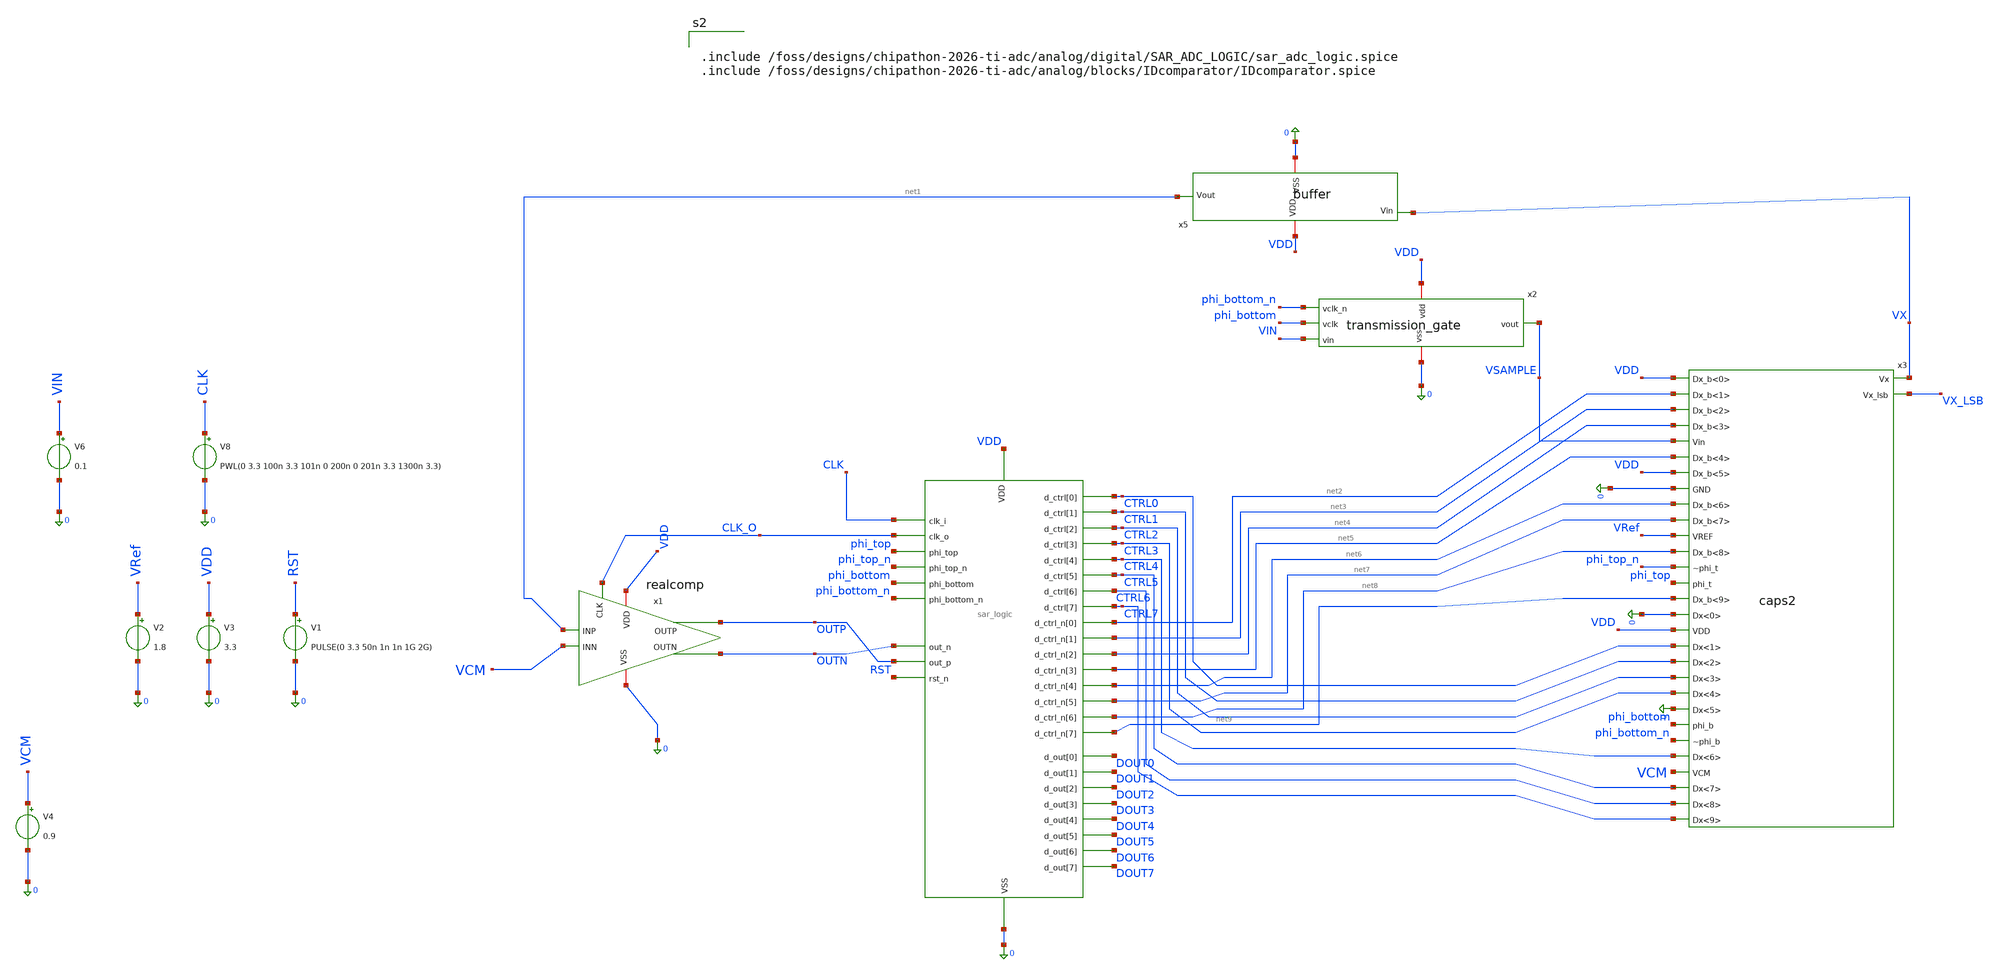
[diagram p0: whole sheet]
** sch_path: analog/top/toptest.sch
**.subckt toptest
V8 CLK 0 PWL(0 3.3 100n 3.3 101n 0 200n 0 201n 3.3 1300n 3.3)
V3 VDD 0 3.3
V1 RST 0 PULSE(0 3.3 50n 1n 1n 1G 2G)
V6 VIN 0 0.1
V2 VRef 0 1.8
V4 VCM 0 0.9
x2 VDD VSAMPLE phi_bottom_n phi_bottom VIN 0 transmission_gate
x3 VDD net2 net3 net4 VSAMPLE net5 VDD 0 net6 net7 VRef net8 phi_top_n phi_top net9 0 VDD CTRL0 VX
+ CTRL1 CTRL2 VX_LSB CTRL3 0 phi_bottom phi_bottom_n CTRL4 VCM CTRL5 CTRL6 CTRL7 caps2
X4 VDD 0 CLK CLK_O CTRL0 CTRL1 CTRL2 CTRL3 CTRL4 CTRL5 CTRL6 CTRL7 net2 net3 net4 net5 net6 net7
+ net8 net9 DOUT0 DOUT1 DOUT2 DOUT3 DOUT4 DOUT5 DOUT6 DOUT7 OUTN OUTP phi_bottom phi_bottom_n phi_top
+ phi_top_n RST sar_adc_logic
x5 VDD VX net1 0 buffer
x1 OUTN OUTP CLK_O 0 VDD net1 VCM realcomp
**** begin user architecture code


.include /foss/designs/chipathon-2026-ti-adc/analog/digital/SAR_ADC_LOGIC/sar_adc_logic.spice
.include /foss/designs/chipathon-2026-ti-adc/analog/blocks/IDcomparator/IDcomparator.spice



.include $::180MCU_MODELS/design.ngspice
.include $PDK_ROOT/gf180mcuD/libs.ref/gf180mcu_fd_sc_mcu7t5v0/spice/gf180mcu_fd_sc_mcu7t5v0.spice
.lib $::180MCU_MODELS/sm141064.ngspice typical
.lib $::180MCU_MODELS/smbb000149.ngspice typical
.lib /foss/pdks/gf180mcuD/libs.tech/ngspice/sm141064.ngspice cap_mim
.lib /foss/pdks/gf180mcuD/libs.tech/ngspice/sm141064.ngspice mimcap_typical



.tran 10n 450n uic
.ic v(VX)=1.65 v(VX_LSB)=1.65

.control
set method=gear
set reltol=1e-3
run
wrdata trans_gate.txt v(vin) v(vsample) v(clk) v(phi_bottom)
wrdata comparator.txt v(clk_o) v(outp) v(outn) v(clk)
wrdata logic.txt v(ctrl0) v(ctrl1) v(ctrl2) v(ctrl3) v(ctrl4) v(ctrl5) v(ctrl6) v(ctrl7) v(dout0)
+ v(dout1) v(dout2) v(dout3) v(dout4) v(dout5) v(dout6) v(dout7) v(clk) v(phi_top) v(phi_bottom) v(rst)
wrdata cdac.txt v(vref) v(vx) v(vcm) v(vsample) v(phi_top) v(phi_bottom)
.endc


**** end user architecture code
**.ends
.end
